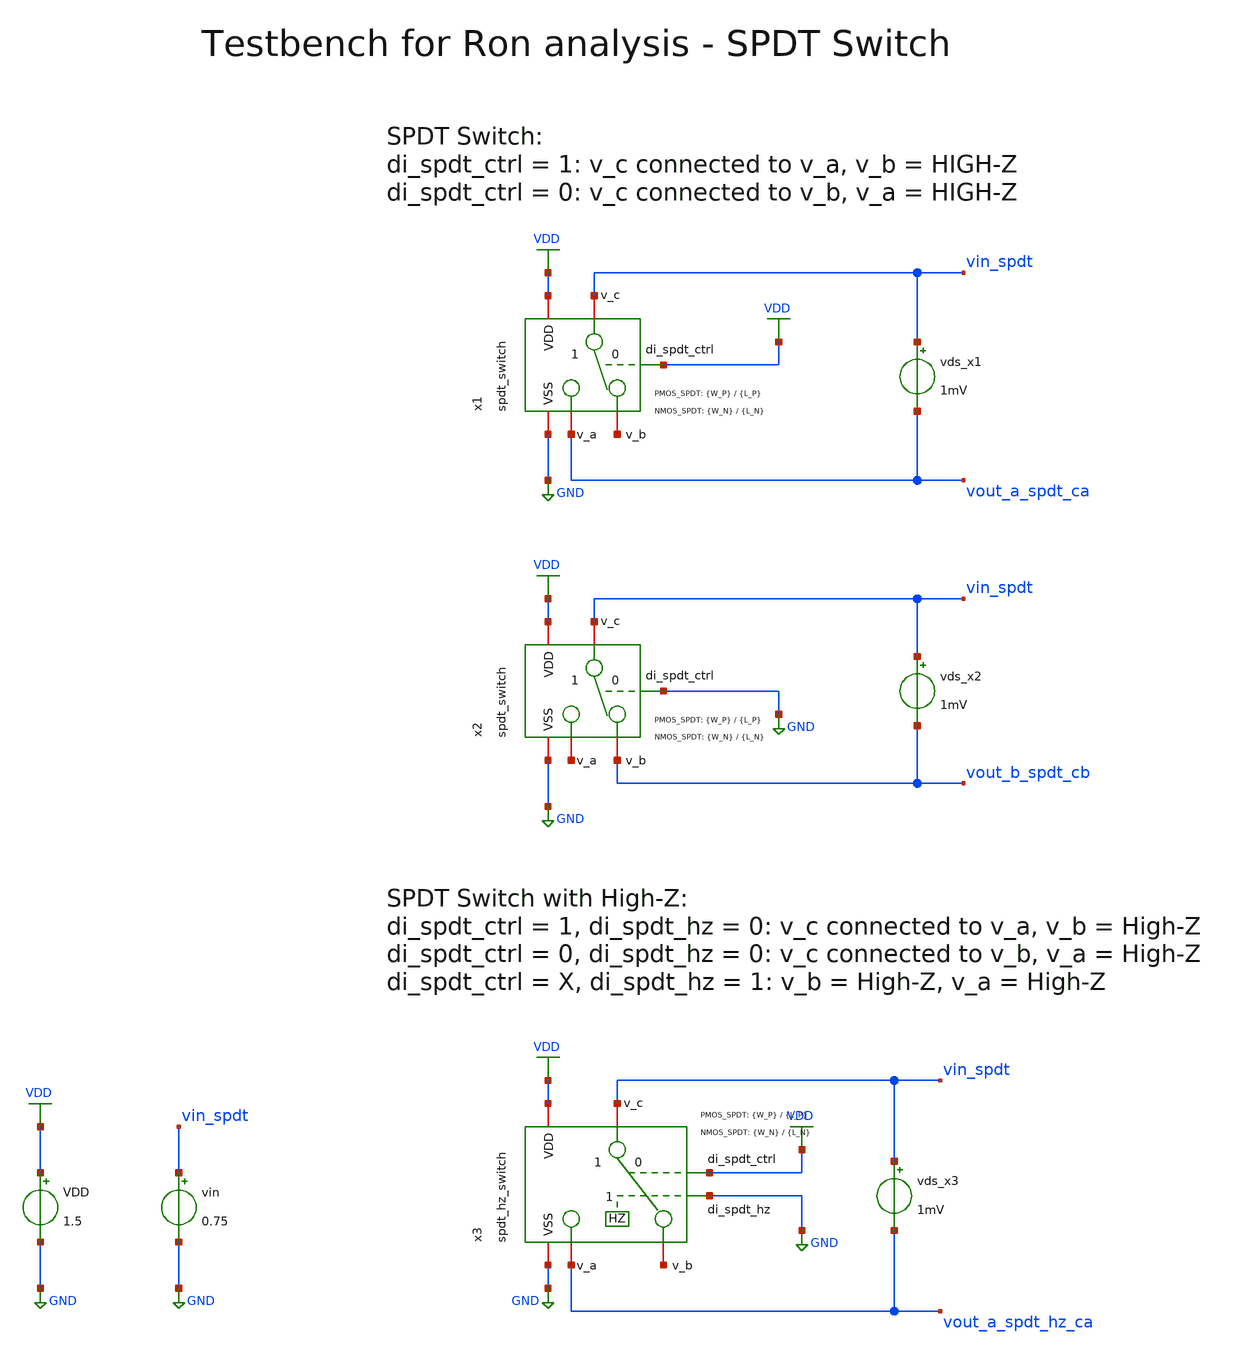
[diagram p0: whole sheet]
** sch_path: SG13G2_ATBS-ADC-main/xschem/spdt_switch/testbenches/spdt_switch_tb_dc_Ron.sch
**.subckt spdt_switch_tb_dc_Ron
vds_x1 vin_spdt vout_a_spdt_ca 1mV
vds_x2 vin_spdt vout_b_spdt_cb 1mV
VDD VDD GND 1.5
vin vin_spdt GND 0.75
x1 VDD VDD GND vin_spdt net1 vout_a_spdt_ca spdt_switch W_P_TG={W_P} L_P_TG={L_P} W_N_TG={W_N} L_N_TG={L_N}
x2 VDD GND GND vin_spdt vout_b_spdt_cb net2 spdt_switch W_P_TG={W_P} L_P_TG={L_P} W_N_TG={W_N} L_N_TG={L_N}
x3 VDD VDD GND vin_spdt net3 vout_a_spdt_hz_ca GND spdt_hz_switch W_P_TG={W_P} L_P_TG={L_P} W_N_TG={W_N}
+ L_N_TG={L_N}
vds_x3 vin_spdt vout_a_spdt_hz_ca 1mV
**** begin user architecture code

.lib cornerMOSlv.lib mos_tt
.lib cornerRES.lib res_typ



.param temp=27
.param W_N=1u
.param L_N=0.13u
.param W_P=1u
.param L_P=0.13u
.options savecurrents
.control
save all

* Operating Point Analysis
op
remzerovec
write spdt_switch_tb_dc_Ron.raw
set appendwrite

* DC Sweep Analysis
dc vin 0 1.5 0.01
write spdt_switch_tb_dc_Ron.raw

* On-Resistance v_c to v_a
let r_on_ca = (v(vout_a_spdt_ca)-v(vin_spdt))/I(vds_x1)
plot r_on_ca xlabel 'Vin in V' ylabel 'Ron in Ohm'

* On-Resistance v_c to v_b
let r_on_cb = (v(vout_b_spdt_cb)-v(vin_spdt))/I(vds_x2)
plot r_on_cb xlabel 'Vin in V' ylabel 'Ron in Ohm'

* On-Resistance v_c to v_a with High-Z TG
let r_on_ca = (v(vout_a_spdt_hz_ca)-v(vin_spdt))/I(vds_x3)
plot r_on_ca xlabel 'Vin in V' ylabel 'Ron in Ohm'

*quit
.endc

**** end user architecture code
**.ends

* expanding   symbol:  spdt_switch/spdt_switch.sym # of pins=6
** sym_path: SG13G2_ATBS-ADC-main/xschem/spdt_switch/spdt_switch.sym
** sch_path: SG13G2_ATBS-ADC-main/xschem/spdt_switch/spdt_switch.sch
.subckt spdt_switch VDD di_spdt_ctrl VSS v_c v_b v_a  W_P_TG=3.0u L_P_TG=0.13u W_N_TG=1.0u
+ L_N_TG=0.13u
*.iopin v_a
*.iopin v_b
*.iopin v_c
*.iopin VDD
*.iopin VSS
*.ipin di_spdt_ctrl
x1 VDD di_spdt_ctrl VSS v_c v_a di_spdt_ctrl_n transmission_gate_lv_wo_dummy W_P=W_P_TG L_P=L_P_TG
+ W_N=W_N_TG L_N=L_N_TG
x2 VDD di_spdt_ctrl_n VSS v_b v_c di_spdt_ctrl transmission_gate_lv_wo_dummy W_P=W_P_TG L_P=L_P_TG
+ W_N=W_N_TG L_N=L_N_TG
x8 VDD di_spdt_ctrl di_spdt_ctrl_n VSS inverter_lv W_P=W_P_TG L_P=L_P_TG W_N=W_N_TG L_N=L_N_TG
.ends


* expanding   symbol:  spdt_switch/spdt_hz_switch.sym # of pins=7
** sym_path: SG13G2_ATBS-ADC-main/xschem/spdt_switch/spdt_hz_switch.sym
** sch_path: SG13G2_ATBS-ADC-main/xschem/spdt_switch/spdt_hz_switch.sch
.subckt spdt_hz_switch VDD di_spdt_ctrl VSS v_c v_b v_a di_spdt_hz  W_P_TG=3.0u L_P_TG=0.13u
+ W_N_TG=1.0u L_N_TG=0.13u
*.iopin v_a
*.iopin v_b
*.iopin v_c
*.iopin VDD
*.iopin VSS
*.ipin di_spdt_ctrl
*.ipin di_spdt_hz
x1 VDD di_spdt_ctrl VSS net1 v_a di_spdt_ctrl_n transmission_gate_lv_wo_dummy W_P=W_P_TG L_P=L_P_TG
+ W_N=W_N_TG L_N=L_N_TG
x2 VDD di_spdt_ctrl_n VSS v_b net1 di_spdt_ctrl transmission_gate_lv_wo_dummy W_P=W_P_TG L_P=L_P_TG
+ W_N=W_N_TG L_N=L_N_TG
x8 VDD di_spdt_ctrl di_spdt_ctrl_n VSS inverter_lv W_P=W_P_TG L_P=L_P_TG W_N=W_N_TG L_N=L_N_TG
x3 VDD di_spdt_hz di_spdt_hz_n VSS inverter_lv W_P=W_P_TG L_P=L_P_TG W_N=W_N_TG L_N=L_N_TG
x4 VDD di_spdt_hz_n VSS v_c net1 di_spdt_hz transmission_gate_lv_wo_dummy W_P=W_P_TG L_P=L_P_TG
+ W_N=W_N_TG L_N=L_N_TG
.ends


* expanding   symbol:  transmission_gate/transmission_gate_lv_wo_dummy.sym # of pins=6
** sym_path: SG13G2_ATBS-ADC-main/xschem/transmission_gate/transmission_gate_lv_wo_dummy.sym
** sch_path: SG13G2_ATBS-ADC-main/xschem/transmission_gate/transmission_gate_lv_wo_dummy.sch
.subckt transmission_gate_lv_wo_dummy VDD di_tg_ctrl VSS v_b v_a di_tg_ctrl_n  W_P=1.0u L_P=0.13u
+ W_N=1.0u L_N=0.13u
*.iopin v_a
*.iopin v_b
*.iopin VDD
*.iopin VSS
*.ipin di_tg_ctrl
*.ipin di_tg_ctrl_n
XM1 v_a di_tg_ctrl v_b VSS sg13_lv_nmos w=W_N l=L_N ng=1 m=1 mm_ok=1
XM2 v_a di_tg_ctrl_n v_b VDD sg13_lv_pmos w=W_P l=L_P ng=1 m=1 mm_ok=1
.ends


* expanding   symbol:  inverter/inverter_lv.sym # of pins=4
** sym_path: SG13G2_ATBS-ADC-main/xschem/inverter/inverter_lv.sym
** sch_path: SG13G2_ATBS-ADC-main/xschem/inverter/inverter_lv.sch
.subckt inverter_lv VDD vin vout VSS  W_P=3.0u L_P=0.13u W_N=1.0u L_N=0.13u
*.ipin vin
*.iopin VDD
*.iopin VSS
*.opin vout
XM1 vout vin VDD VDD sg13_lv_pmos w=W_P l=L_P ng=1 m=1 mm_ok=1
XM2 vout vin VSS VSS sg13_lv_nmos w=W_N l=L_N ng=1 m=1 mm_ok=1
.ends

.GLOBAL VDD
.GLOBAL GND
.end
